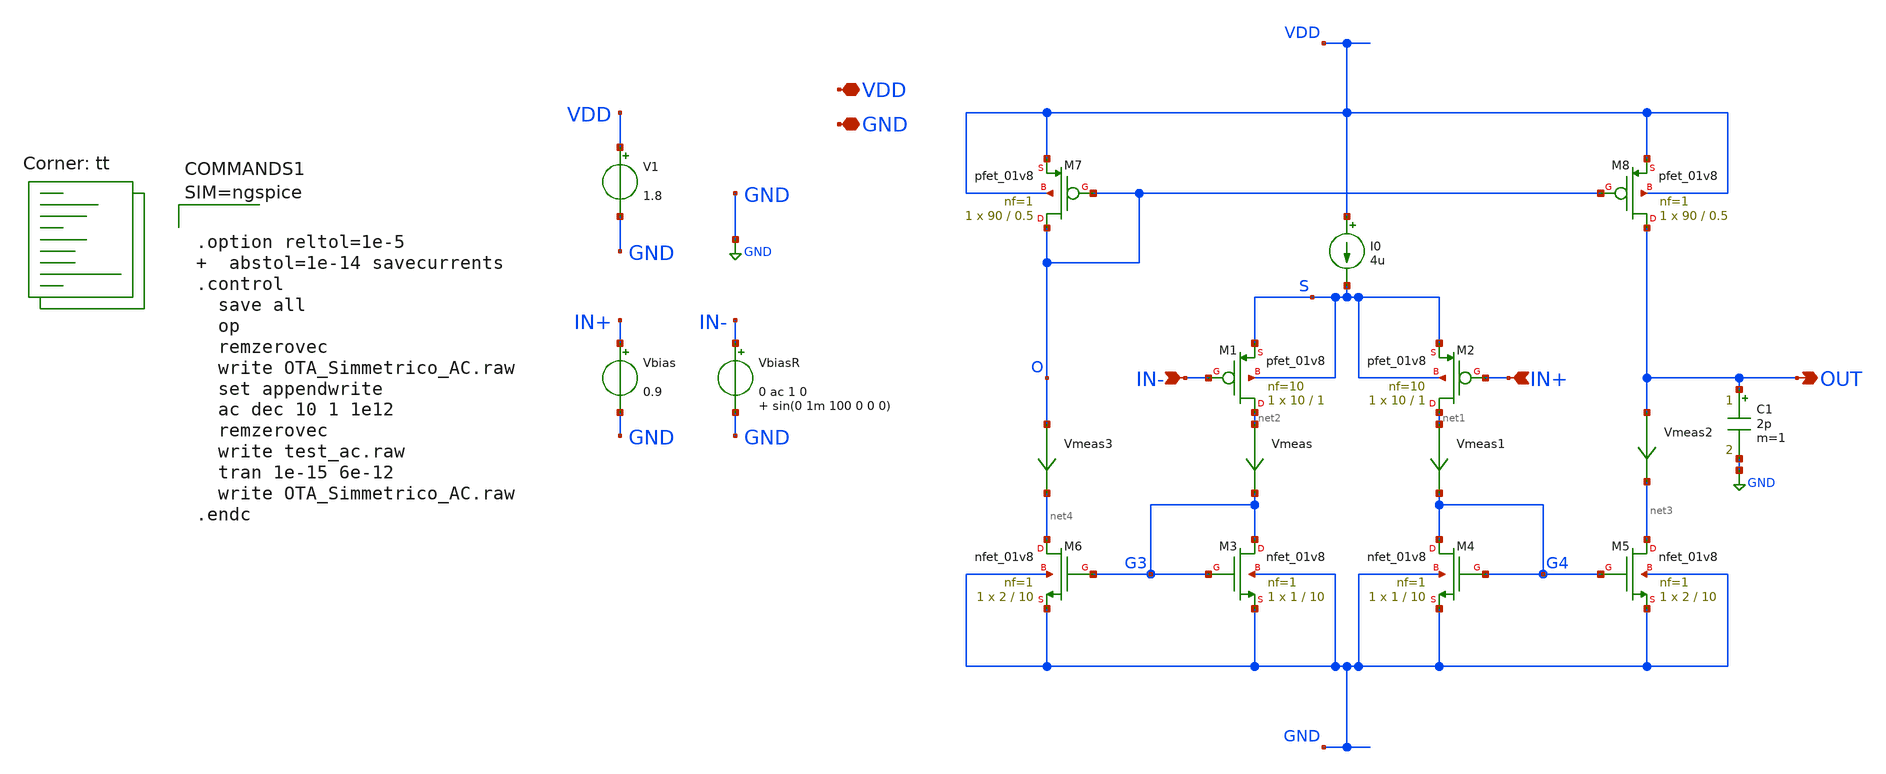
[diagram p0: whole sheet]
** sch_path: xschem/OTA_Simmetrico_AC.sch
**.subckt OTA_Simmetrico_AC VDD GND OUT IN+ IN-
*.iopin VDD
*.iopin GND
*.opin OUT
*.ipin IN+
*.ipin IN-
V1 VDD GND 1.8
Vbias IN+ GND 0.9
VbiasR IN- GND 0 ac 1 0 sin(0 1m 100 0 0 0)
C1 OUT GND 2p m=1
XM1 net2 IN- S S sky130_fd_pr__pfet_01v8 L=1 W=10 nf=10 ad='int((nf+1)/2) * W/nf * 0.29' as='int((nf+2)/2) * W/nf * 0.29'
+ pd='2*int((nf+1)/2) * (W/nf + 0.29)' ps='2*int((nf+2)/2) * (W/nf + 0.29)' nrd='0.29 / W' nrs='0.29 / W'
+ sa=0 sb=0 sd=0 mult=1 m=1
XM2 net1 IN+ S S sky130_fd_pr__pfet_01v8 L=1 W=10 nf=10 ad='int((nf+1)/2) * W/nf * 0.29' as='int((nf+2)/2) * W/nf * 0.29'
+ pd='2*int((nf+1)/2) * (W/nf + 0.29)' ps='2*int((nf+2)/2) * (W/nf + 0.29)' nrd='0.29 / W' nrs='0.29 / W'
+ sa=0 sb=0 sd=0 mult=1 m=1
XM3 G3 G3 GND GND sky130_fd_pr__nfet_01v8 L=10 W=1 nf=1 ad='int((nf+1)/2) * W/nf * 0.29' as='int((nf+2)/2) * W/nf * 0.29'
+ pd='2*int((nf+1)/2) * (W/nf + 0.29)' ps='2*int((nf+2)/2) * (W/nf + 0.29)' nrd='0.29 / W' nrs='0.29 / W'
+ sa=0 sb=0 sd=0 mult=1 m=1
XM4 G4 G4 GND GND sky130_fd_pr__nfet_01v8 L=10 W=1 nf=1 ad='int((nf+1)/2) * W/nf * 0.29' as='int((nf+2)/2) * W/nf * 0.29'
+ pd='2*int((nf+1)/2) * (W/nf + 0.29)' ps='2*int((nf+2)/2) * (W/nf + 0.29)' nrd='0.29 / W' nrs='0.29 / W'
+ sa=0 sb=0 sd=0 mult=1 m=1
XM5 net3 G4 GND GND sky130_fd_pr__nfet_01v8 L=10 W=2 nf=1 ad='int((nf+1)/2) * W/nf * 0.29' as='int((nf+2)/2) * W/nf * 0.29'
+ pd='2*int((nf+1)/2) * (W/nf + 0.29)' ps='2*int((nf+2)/2) * (W/nf + 0.29)' nrd='0.29 / W' nrs='0.29 / W'
+ sa=0 sb=0 sd=0 mult=1 m=1
XM6 net4 G3 GND GND sky130_fd_pr__nfet_01v8 L=10 W=2 nf=1 ad='int((nf+1)/2) * W/nf * 0.29' as='int((nf+2)/2) * W/nf * 0.29'
+ pd='2*int((nf+1)/2) * (W/nf + 0.29)' ps='2*int((nf+2)/2) * (W/nf + 0.29)' nrd='0.29 / W' nrs='0.29 / W'
+ sa=0 sb=0 sd=0 mult=1 m=1
XM7 O O VDD VDD sky130_fd_pr__pfet_01v8 L=0.5 W=90 nf=1 ad='int((nf+1)/2) * W/nf * 0.29' as='int((nf+2)/2) * W/nf * 0.29'
+ pd='2*int((nf+1)/2) * (W/nf + 0.29)' ps='2*int((nf+2)/2) * (W/nf + 0.29)' nrd='0.29 / W' nrs='0.29 / W'
+ sa=0 sb=0 sd=0 mult=1 m=1
XM8 OUT O VDD VDD sky130_fd_pr__pfet_01v8 L=0.5 W=90 nf=1 ad='int((nf+1)/2) * W/nf * 0.29' as='int((nf+2)/2) * W/nf * 0.29'
+ pd='2*int((nf+1)/2) * (W/nf + 0.29)' ps='2*int((nf+2)/2) * (W/nf + 0.29)' nrd='0.29 / W' nrs='0.29 / W'
+ sa=0 sb=0 sd=0 mult=1 m=1
I0 VDD S 4u
Vmeas net2 G3 0
.save i(vmeas)
Vmeas1 net1 G4 0
.save i(vmeas1)
Vmeas2 OUT net3 0
.save i(vmeas2)
Vmeas3 O net4 0
.save i(vmeas3)
**** begin user architecture code
.lib $::SKYWATER_MODELS/sky130.lib.spice tt



.option reltol=1e-5   abstol=1e-14 savecurrents
.control
  save all
  op
  remzerovec
  write OTA_Simmetrico_AC.raw
  set appendwrite
  ac dec 10 1 1e12
  remzerovec
  write test_ac.raw
  tran 1e-15 6e-12
  write OTA_Simmetrico_AC.raw
.endc



**** end user architecture code
**.ends
.GLOBAL GND
.end
